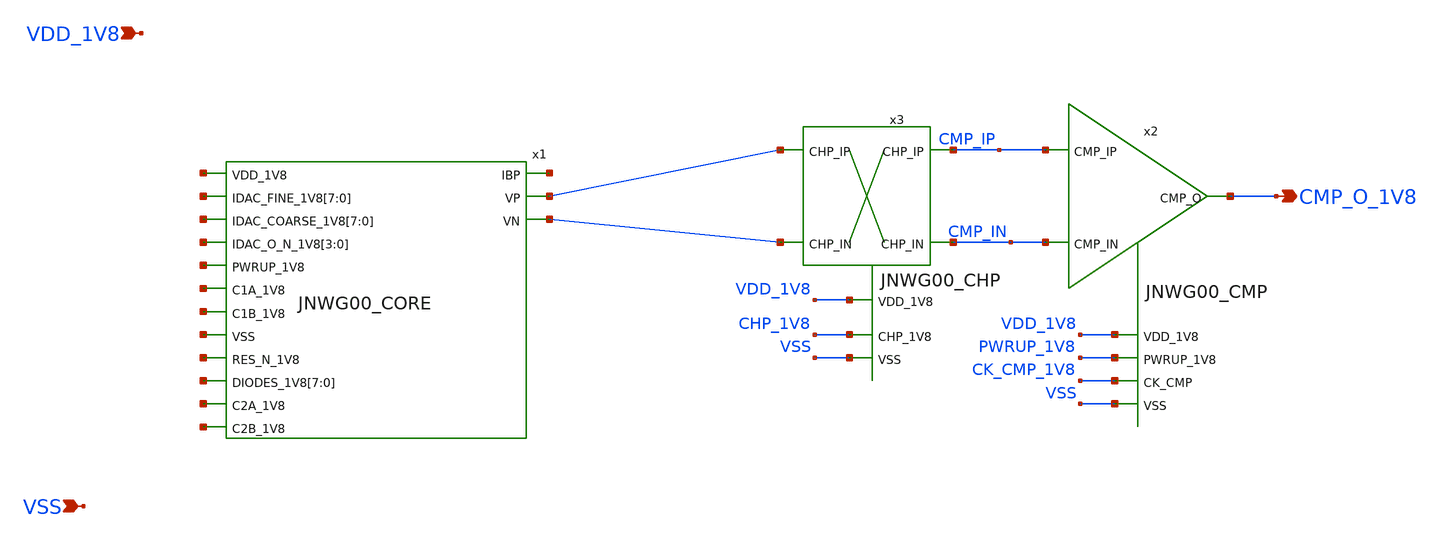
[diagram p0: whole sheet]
** sch_path: design/JNW_GR00_SKY130NM/JNWG00_ANA.sch
**.subckt JNWG00_ANA VDD_1V8 VSS CMP_O_1V8
*.ipin VDD_1V8
*.ipin VSS
*.opin CMP_O_1V8
x2 VDD_1V8 PWRUP_1V8 CMP_IP CMP_O_1V8 CMP_IN CK_CMP_1V8 VSS JNWG00_CMP
x3 VDD_1V8 CMP_IP CMP_IN CHP_1V8 VSS JNWG00_CHP
x1 net1 net2[7] net2[6] net2[5] net2[4] net2[3] net2[2] net2[1] net2[0] net3[7] net3[6] net3[5]
+ net3[4] net3[3] net3[2] net3[1] net3[0] net4[3] net4[2] net4[1] net4[0] net5 net6 net7 CMP_IP net8 net9
+ net10 net11[7] net11[6] net11[5] net11[4] net11[3] net11[2] net11[1] net11[0] CMP_IN net12 net13
+ JNWG00_CORE
**.ends
.end
